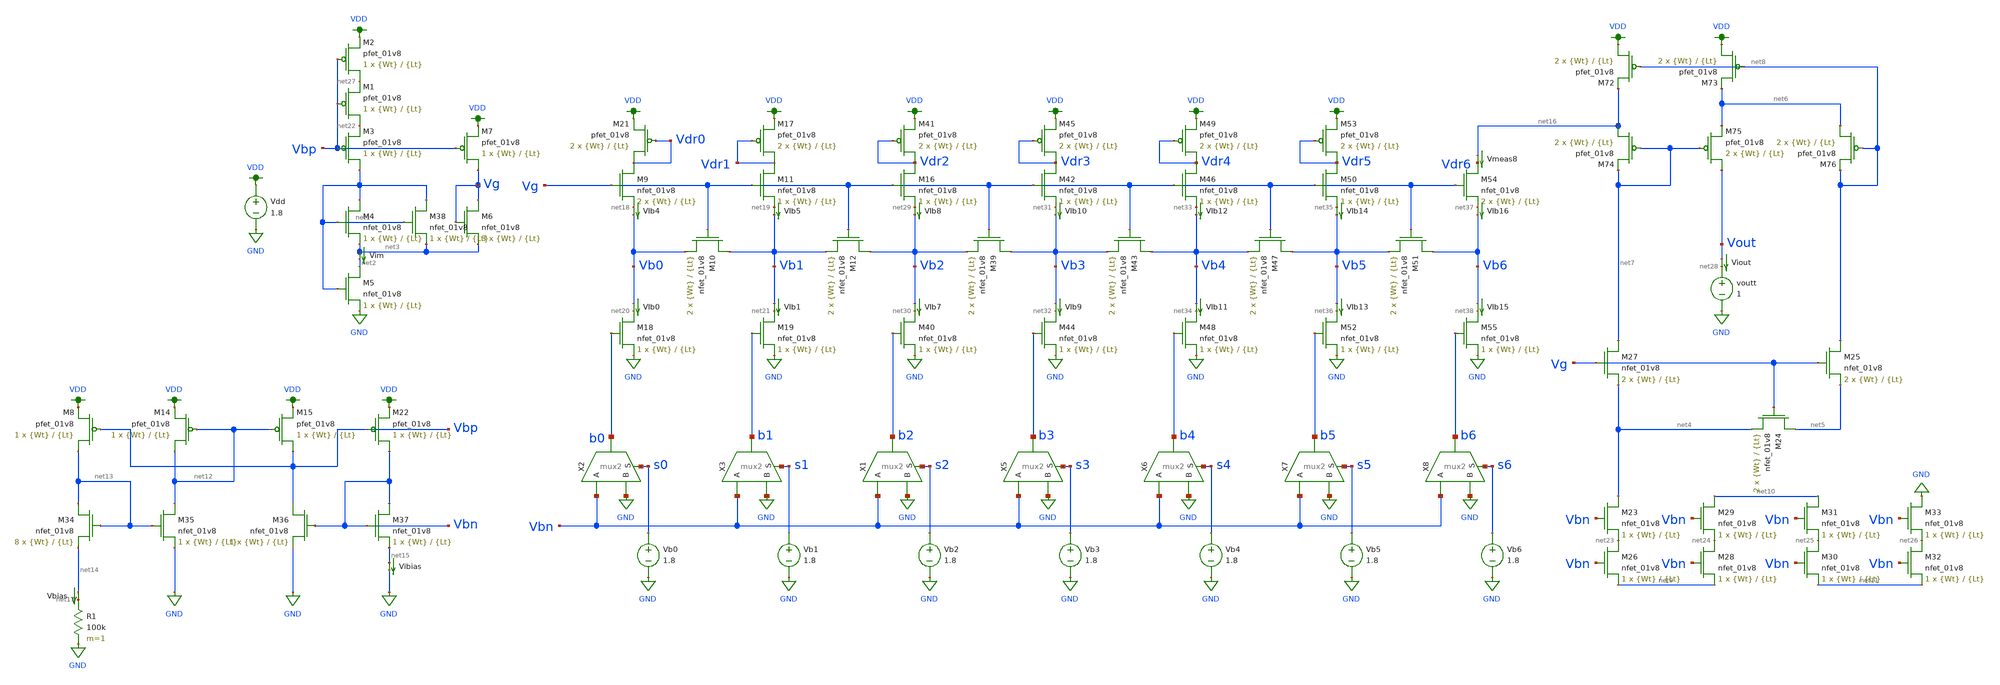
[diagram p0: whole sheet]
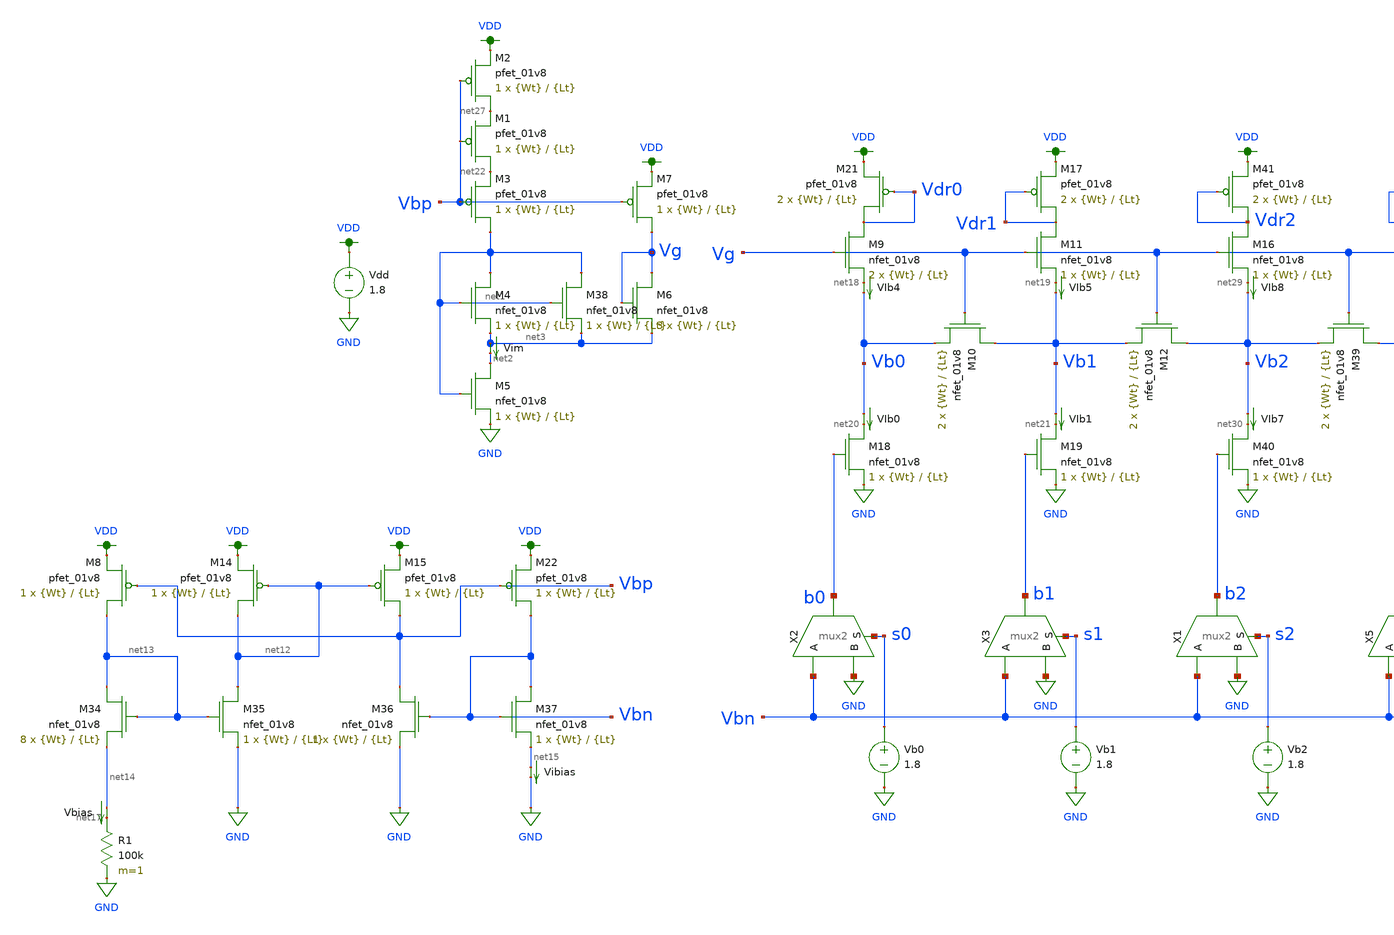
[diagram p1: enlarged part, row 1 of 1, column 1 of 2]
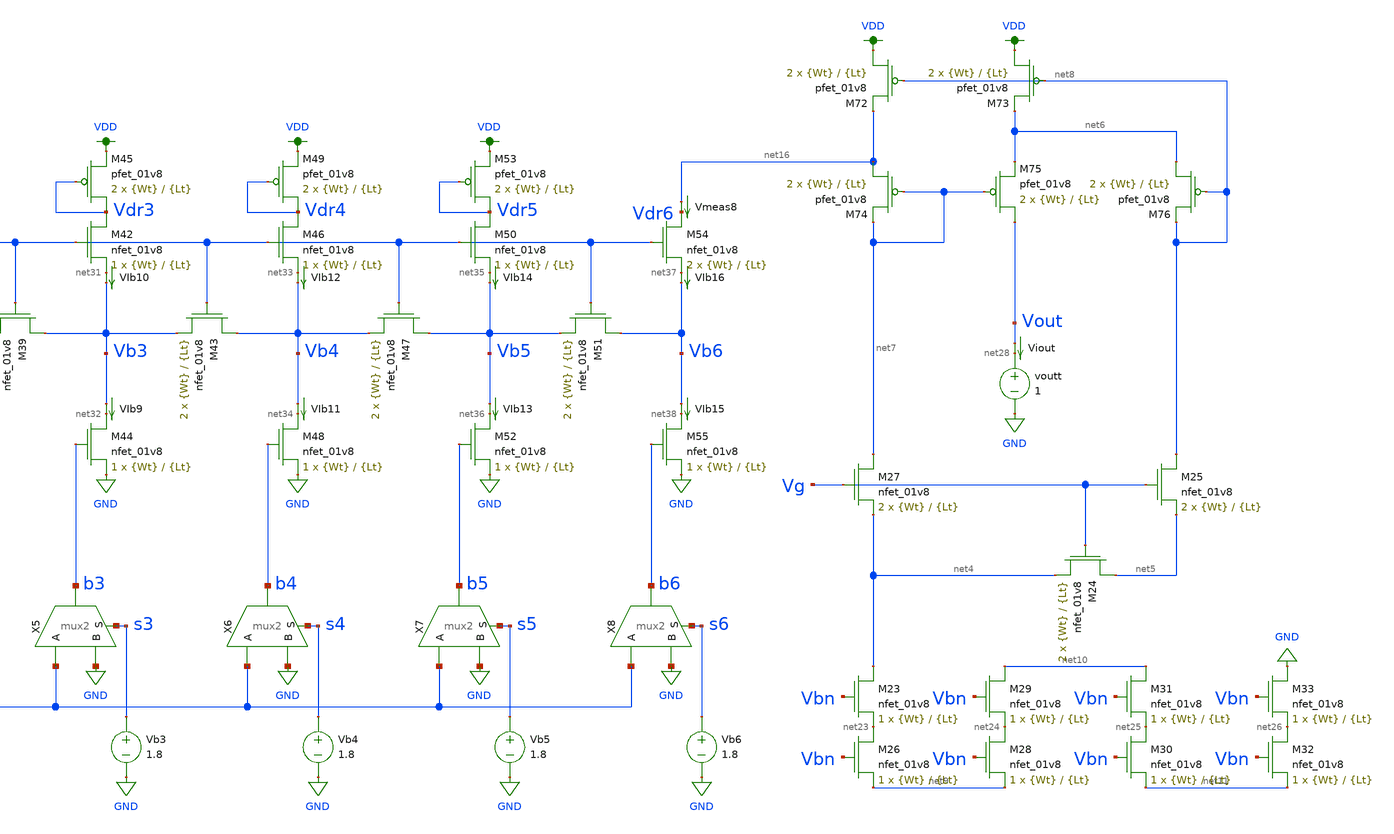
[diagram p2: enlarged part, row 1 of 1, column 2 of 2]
** sch_path: schematic/archive/dac7_test_SL.sch
**.subckt dac7_test_SL
X2 b0 Vbn GND s0 mux2
X3 b1 Vbn GND s1 mux2
R1 net17 GND 100k m=1
Vdd VDD GND 1.8
Vb0 s0 GND 1.8
Vb1 s1 GND 1.8
XM9 Vdr0 Vg net18 GND sky130_fd_pr__nfet_01v8 L={Lt} W={Wt} nf=1 ad='int((nf+1)/2) * W/nf * 0.29' as='int((nf+2)/2) * W/nf * 0.29'
+ pd='2*int((nf+1)/2) * (W/nf + 0.29)' ps='2*int((nf+2)/2) * (W/nf + 0.29)' nrd='0.29 / W' nrs='0.29 / W'
+ sa=0 sb=0 sd=0 mult=2 m=2
XM10 Vb1 Vg Vb0 GND sky130_fd_pr__nfet_01v8 L={Lt} W={Wt} nf=1 ad='int((nf+1)/2) * W/nf * 0.29' as='int((nf+2)/2) * W/nf * 0.29'
+ pd='2*int((nf+1)/2) * (W/nf + 0.29)' ps='2*int((nf+2)/2) * (W/nf + 0.29)' nrd='0.29 / W' nrs='0.29 / W'
+ sa=0 sb=0 sd=0 mult=2 m=2
XM11 Vdr1 Vg net19 GND sky130_fd_pr__nfet_01v8 L={Lt} W={Wt} nf=1 ad='int((nf+1)/2) * W/nf * 0.29' as='int((nf+2)/2) * W/nf * 0.29'
+ pd='2*int((nf+1)/2) * (W/nf + 0.29)' ps='2*int((nf+2)/2) * (W/nf + 0.29)' nrd='0.29 / W' nrs='0.29 / W'
+ sa=0 sb=0 sd=0 mult=1 m=1
XM12 Vb2 Vg Vb1 GND sky130_fd_pr__nfet_01v8 L={Lt} W={Wt} nf=1 ad='int((nf+1)/2) * W/nf * 0.29' as='int((nf+2)/2) * W/nf * 0.29'
+ pd='2*int((nf+1)/2) * (W/nf + 0.29)' ps='2*int((nf+2)/2) * (W/nf + 0.29)' nrd='0.29 / W' nrs='0.29 / W'
+ sa=0 sb=0 sd=0 mult=2 m=2
XM18 net20 b0 GND GND sky130_fd_pr__nfet_01v8 L={Lt} W={Wt} nf=1 ad='int((nf+1)/2) * W/nf * 0.29' as='int((nf+2)/2) * W/nf * 0.29'
+ pd='2*int((nf+1)/2) * (W/nf + 0.29)' ps='2*int((nf+2)/2) * (W/nf + 0.29)' nrd='0.29 / W' nrs='0.29 / W'
+ sa=0 sb=0 sd=0 mult=1 m=1
XM19 net21 b1 GND GND sky130_fd_pr__nfet_01v8 L={Lt} W={Wt} nf=1 ad='int((nf+1)/2) * W/nf * 0.29' as='int((nf+2)/2) * W/nf * 0.29'
+ pd='2*int((nf+1)/2) * (W/nf + 0.29)' ps='2*int((nf+2)/2) * (W/nf + 0.29)' nrd='0.29 / W' nrs='0.29 / W'
+ sa=0 sb=0 sd=0 mult=1 m=1
Vbias net14 net17 0
.save i(vbias)
VIb0 Vb0 net20 0
.save i(vib0)
VIb1 Vb1 net21 0
.save i(vib1)
XM3 net1 Vbp net22 VDD sky130_fd_pr__pfet_01v8 L={Lt} W={Wt} nf=1 ad='int((nf+1)/2) * W/nf * 0.29' as='int((nf+2)/2) * W/nf * 0.29'
+ pd='2*int((nf+1)/2) * (W/nf + 0.29)' ps='2*int((nf+2)/2) * (W/nf + 0.29)' nrd='0.29 / W' nrs='0.29 / W'
+ sa=0 sb=0 sd=0 mult=1 m=1
XM4 net1 net1 net3 GND sky130_fd_pr__nfet_01v8 L={Lt} W={Wt} nf=1 ad='int((nf+1)/2) * W/nf * 0.29' as='int((nf+2)/2) * W/nf * 0.29'
+ pd='2*int((nf+1)/2) * (W/nf + 0.29)' ps='2*int((nf+2)/2) * (W/nf + 0.29)' nrd='0.29 / W' nrs='0.29 / W'
+ sa=0 sb=0 sd=0 mult=1 m=1
XM5 net2 net1 GND GND sky130_fd_pr__nfet_01v8 L={Lt} W={Wt} nf=1 ad='int((nf+1)/2) * W/nf * 0.29' as='int((nf+2)/2) * W/nf * 0.29'
+ pd='2*int((nf+1)/2) * (W/nf + 0.29)' ps='2*int((nf+2)/2) * (W/nf + 0.29)' nrd='0.29 / W' nrs='0.29 / W'
+ sa=0 sb=0 sd=0 mult=1 m=1
Vim net3 net2 0
.save i(vim)
XM6 Vg Vg net3 GND sky130_fd_pr__nfet_01v8 L={Lt} W={Wt} nf=1 ad='int((nf+1)/2) * W/nf * 0.29' as='int((nf+2)/2) * W/nf * 0.29'
+ pd='2*int((nf+1)/2) * (W/nf + 0.29)' ps='2*int((nf+2)/2) * (W/nf + 0.29)' nrd='0.29 / W' nrs='0.29 / W'
+ sa=0 sb=0 sd=0 mult=3 m=3
XM7 Vg Vbp VDD VDD sky130_fd_pr__pfet_01v8 L={Lt} W={Wt} nf=1 ad='int((nf+1)/2) * W/nf * 0.29' as='int((nf+2)/2) * W/nf * 0.29'
+ pd='2*int((nf+1)/2) * (W/nf + 0.29)' ps='2*int((nf+2)/2) * (W/nf + 0.29)' nrd='0.29 / W' nrs='0.29 / W'
+ sa=0 sb=0 sd=0 mult=1 m=1
XM17 Vdr1 Vdr1 VDD VDD sky130_fd_pr__pfet_01v8 L={Lt} W={Wt} nf=1 ad='int((nf+1)/2) * W/nf * 0.29' as='int((nf+2)/2) * W/nf * 0.29'
+ pd='2*int((nf+1)/2) * (W/nf + 0.29)' ps='2*int((nf+2)/2) * (W/nf + 0.29)' nrd='0.29 / W' nrs='0.29 / W'
+ sa=0 sb=0 sd=0 mult=2 m=2
XM21 Vdr0 Vdr0 VDD VDD sky130_fd_pr__pfet_01v8 L={Lt} W={Wt} nf=1 ad='int((nf+1)/2) * W/nf * 0.29' as='int((nf+2)/2) * W/nf * 0.29'
+ pd='2*int((nf+1)/2) * (W/nf + 0.29)' ps='2*int((nf+2)/2) * (W/nf + 0.29)' nrd='0.29 / W' nrs='0.29 / W'
+ sa=0 sb=0 sd=0 mult=2 m=2
VIb4 net18 Vb0 0
.save i(vib4)
VIb5 net19 Vb1 0
.save i(vib5)
XM24 net5 Vg net4 GND sky130_fd_pr__nfet_01v8 L={Lt} W={Wt} nf=1 ad='int((nf+1)/2) * W/nf * 0.29' as='int((nf+2)/2) * W/nf * 0.29'
+ pd='2*int((nf+1)/2) * (W/nf + 0.29)' ps='2*int((nf+2)/2) * (W/nf + 0.29)' nrd='0.29 / W' nrs='0.29 / W'
+ sa=0 sb=0 sd=0 mult=2 m=2
XM25 net8 Vg net5 GND sky130_fd_pr__nfet_01v8 L={Lt} W={Wt} nf=1 ad='int((nf+1)/2) * W/nf * 0.29' as='int((nf+2)/2) * W/nf * 0.29'
+ pd='2*int((nf+1)/2) * (W/nf + 0.29)' ps='2*int((nf+2)/2) * (W/nf + 0.29)' nrd='0.29 / W' nrs='0.29 / W'
+ sa=0 sb=0 sd=0 mult=2 m=2
XM26 net23 Vbn net9 GND sky130_fd_pr__nfet_01v8 L={Lt} W={Wt} nf=1 ad='int((nf+1)/2) * W/nf * 0.29' as='int((nf+2)/2) * W/nf * 0.29'
+ pd='2*int((nf+1)/2) * (W/nf + 0.29)' ps='2*int((nf+2)/2) * (W/nf + 0.29)' nrd='0.29 / W' nrs='0.29 / W'
+ sa=0 sb=0 sd=0 mult=1 m=1
XM27 net7 Vg net4 GND sky130_fd_pr__nfet_01v8 L={Lt} W={Wt} nf=1 ad='int((nf+1)/2) * W/nf * 0.29' as='int((nf+2)/2) * W/nf * 0.29'
+ pd='2*int((nf+1)/2) * (W/nf + 0.29)' ps='2*int((nf+2)/2) * (W/nf + 0.29)' nrd='0.29 / W' nrs='0.29 / W'
+ sa=0 sb=0 sd=0 mult=2 m=2
XM72 VDD net8 net16 VDD sky130_fd_pr__pfet_01v8 L={Lt} W={Wt} nf=1 ad='int((nf+1)/2) * W/nf * 0.29' as='int((nf+2)/2) * W/nf * 0.29'
+ pd='2*int((nf+1)/2) * (W/nf + 0.29)' ps='2*int((nf+2)/2) * (W/nf + 0.29)' nrd='0.29 / W' nrs='0.29 / W'
+ sa=0 sb=0 sd=0 mult=2 m=2
XM73 VDD net8 net6 VDD sky130_fd_pr__pfet_01v8 L={Lt} W={Wt} nf=1 ad='int((nf+1)/2) * W/nf * 0.29' as='int((nf+2)/2) * W/nf * 0.29'
+ pd='2*int((nf+1)/2) * (W/nf + 0.29)' ps='2*int((nf+2)/2) * (W/nf + 0.29)' nrd='0.29 / W' nrs='0.29 / W'
+ sa=0 sb=0 sd=0 mult=2 m=2
XM74 net16 net7 net7 VDD sky130_fd_pr__pfet_01v8 L={Lt} W={Wt} nf=1 ad='int((nf+1)/2) * W/nf * 0.29'
+ as='int((nf+2)/2) * W/nf * 0.29' pd='2*int((nf+1)/2) * (W/nf + 0.29)' ps='2*int((nf+2)/2) * (W/nf + 0.29)'
+ nrd='0.29 / W' nrs='0.29 / W' sa=0 sb=0 sd=0 mult=2 m=2
XM75 Vout net7 net6 VDD sky130_fd_pr__pfet_01v8 L={Lt} W={Wt} nf=1 ad='int((nf+1)/2) * W/nf * 0.29' as='int((nf+2)/2) * W/nf * 0.29'
+ pd='2*int((nf+1)/2) * (W/nf + 0.29)' ps='2*int((nf+2)/2) * (W/nf + 0.29)' nrd='0.29 / W' nrs='0.29 / W'
+ sa=0 sb=0 sd=0 mult=2 m=2
XM76 net6 net8 net8 VDD sky130_fd_pr__pfet_01v8 L={Lt} W={Wt} nf=1 ad='int((nf+1)/2) * W/nf * 0.29' as='int((nf+2)/2) * W/nf * 0.29'
+ pd='2*int((nf+1)/2) * (W/nf + 0.29)' ps='2*int((nf+2)/2) * (W/nf + 0.29)' nrd='0.29 / W' nrs='0.29 / W'
+ sa=0 sb=0 sd=0 mult=2 m=2
XM23 net4 Vbn net23 GND sky130_fd_pr__nfet_01v8 L={Lt} W={Wt} nf=1 ad='int((nf+1)/2) * W/nf * 0.29' as='int((nf+2)/2) * W/nf * 0.29'
+ pd='2*int((nf+1)/2) * (W/nf + 0.29)' ps='2*int((nf+2)/2) * (W/nf + 0.29)' nrd='0.29 / W' nrs='0.29 / W'
+ sa=0 sb=0 sd=0 mult=1 m=1
XM28 net24 Vbn net9 GND sky130_fd_pr__nfet_01v8 L={Lt} W={Wt} nf=1 ad='int((nf+1)/2) * W/nf * 0.29' as='int((nf+2)/2) * W/nf * 0.29'
+ pd='2*int((nf+1)/2) * (W/nf + 0.29)' ps='2*int((nf+2)/2) * (W/nf + 0.29)' nrd='0.29 / W' nrs='0.29 / W'
+ sa=0 sb=0 sd=0 mult=1 m=1
XM29 net10 Vbn net24 GND sky130_fd_pr__nfet_01v8 L={Lt} W={Wt} nf=1 ad='int((nf+1)/2) * W/nf * 0.29'
+ as='int((nf+2)/2) * W/nf * 0.29' pd='2*int((nf+1)/2) * (W/nf + 0.29)' ps='2*int((nf+2)/2) * (W/nf + 0.29)'
+ nrd='0.29 / W' nrs='0.29 / W' sa=0 sb=0 sd=0 mult=1 m=1
XM30 net25 Vbn net11 GND sky130_fd_pr__nfet_01v8 L={Lt} W={Wt} nf=1 ad='int((nf+1)/2) * W/nf * 0.29'
+ as='int((nf+2)/2) * W/nf * 0.29' pd='2*int((nf+1)/2) * (W/nf + 0.29)' ps='2*int((nf+2)/2) * (W/nf + 0.29)'
+ nrd='0.29 / W' nrs='0.29 / W' sa=0 sb=0 sd=0 mult=1 m=1
XM31 net10 Vbn net25 GND sky130_fd_pr__nfet_01v8 L={Lt} W={Wt} nf=1 ad='int((nf+1)/2) * W/nf * 0.29'
+ as='int((nf+2)/2) * W/nf * 0.29' pd='2*int((nf+1)/2) * (W/nf + 0.29)' ps='2*int((nf+2)/2) * (W/nf + 0.29)'
+ nrd='0.29 / W' nrs='0.29 / W' sa=0 sb=0 sd=0 mult=1 m=1
XM32 net26 Vbn net11 GND sky130_fd_pr__nfet_01v8 L={Lt} W={Wt} nf=1 ad='int((nf+1)/2) * W/nf * 0.29'
+ as='int((nf+2)/2) * W/nf * 0.29' pd='2*int((nf+1)/2) * (W/nf + 0.29)' ps='2*int((nf+2)/2) * (W/nf + 0.29)'
+ nrd='0.29 / W' nrs='0.29 / W' sa=0 sb=0 sd=0 mult=1 m=1
XM33 GND Vbn net26 GND sky130_fd_pr__nfet_01v8 L={Lt} W={Wt} nf=1 ad='int((nf+1)/2) * W/nf * 0.29' as='int((nf+2)/2) * W/nf * 0.29'
+ pd='2*int((nf+1)/2) * (W/nf + 0.29)' ps='2*int((nf+2)/2) * (W/nf + 0.29)' nrd='0.29 / W' nrs='0.29 / W'
+ sa=0 sb=0 sd=0 mult=1 m=1
XM8 net13 Vbp VDD VDD sky130_fd_pr__pfet_01v8 L={Lt} W={Wt} nf=1 ad='int((nf+1)/2) * W/nf * 0.29' as='int((nf+2)/2) * W/nf * 0.29'
+ pd='2*int((nf+1)/2) * (W/nf + 0.29)' ps='2*int((nf+2)/2) * (W/nf + 0.29)' nrd='0.29 / W' nrs='0.29 / W'
+ sa=0 sb=0 sd=0 mult=1 m=1
XM14 net12 net12 VDD VDD sky130_fd_pr__pfet_01v8 L={Lt} W={Wt} nf=1 ad='int((nf+1)/2) * W/nf * 0.29'
+ as='int((nf+2)/2) * W/nf * 0.29' pd='2*int((nf+1)/2) * (W/nf + 0.29)' ps='2*int((nf+2)/2) * (W/nf + 0.29)'
+ nrd='0.29 / W' nrs='0.29 / W' sa=0 sb=0 sd=0 mult=1 m=1
XM15 Vbp net12 VDD VDD sky130_fd_pr__pfet_01v8 L={Lt} W={Wt} nf=1 ad='int((nf+1)/2) * W/nf * 0.29' as='int((nf+2)/2) * W/nf * 0.29'
+ pd='2*int((nf+1)/2) * (W/nf + 0.29)' ps='2*int((nf+2)/2) * (W/nf + 0.29)' nrd='0.29 / W' nrs='0.29 / W'
+ sa=0 sb=0 sd=0 mult=1 m=1
XM22 Vbn Vbp VDD VDD sky130_fd_pr__pfet_01v8 L={Lt} W={Wt} nf=1 ad='int((nf+1)/2) * W/nf * 0.29' as='int((nf+2)/2) * W/nf * 0.29'
+ pd='2*int((nf+1)/2) * (W/nf + 0.29)' ps='2*int((nf+2)/2) * (W/nf + 0.29)' nrd='0.29 / W' nrs='0.29 / W'
+ sa=0 sb=0 sd=0 mult=1 m=1
XM34 net13 net13 net14 GND sky130_fd_pr__nfet_01v8 L={Lt} W={Wt} nf=1 ad='int((nf+1)/2) * W/nf * 0.29'
+ as='int((nf+2)/2) * W/nf * 0.29' pd='2*int((nf+1)/2) * (W/nf + 0.29)' ps='2*int((nf+2)/2) * (W/nf + 0.29)'
+ nrd='0.29 / W' nrs='0.29 / W' sa=0 sb=0 sd=0 mult=8 m=8
XM35 net12 net13 GND GND sky130_fd_pr__nfet_01v8 L={Lt} W={Wt} nf=1 ad='int((nf+1)/2) * W/nf * 0.29'
+ as='int((nf+2)/2) * W/nf * 0.29' pd='2*int((nf+1)/2) * (W/nf + 0.29)' ps='2*int((nf+2)/2) * (W/nf + 0.29)'
+ nrd='0.29 / W' nrs='0.29 / W' sa=0 sb=0 sd=0 mult=1 m=1
XM36 Vbp Vbn GND GND sky130_fd_pr__nfet_01v8 L={Lt} W={Wt} nf=1 ad='int((nf+1)/2) * W/nf * 0.29' as='int((nf+2)/2) * W/nf * 0.29'
+ pd='2*int((nf+1)/2) * (W/nf + 0.29)' ps='2*int((nf+2)/2) * (W/nf + 0.29)' nrd='0.29 / W' nrs='0.29 / W'
+ sa=0 sb=0 sd=0 mult=1 m=1
XM37 Vbn Vbn net15 GND sky130_fd_pr__nfet_01v8 L={Lt} W={Wt} nf=1 ad='int((nf+1)/2) * W/nf * 0.29' as='int((nf+2)/2) * W/nf * 0.29'
+ pd='2*int((nf+1)/2) * (W/nf + 0.29)' ps='2*int((nf+2)/2) * (W/nf + 0.29)' nrd='0.29 / W' nrs='0.29 / W'
+ sa=0 sb=0 sd=0 mult=1 m=1
Vibias net15 GND 0
.save i(vibias)
XM1 net22 Vbp net27 VDD sky130_fd_pr__pfet_01v8 L={Lt} W={Wt} nf=1 ad='int((nf+1)/2) * W/nf * 0.29' as='int((nf+2)/2) * W/nf * 0.29'
+ pd='2*int((nf+1)/2) * (W/nf + 0.29)' ps='2*int((nf+2)/2) * (W/nf + 0.29)' nrd='0.29 / W' nrs='0.29 / W'
+ sa=0 sb=0 sd=0 mult=1 m=1
XM2 net27 Vbp VDD VDD sky130_fd_pr__pfet_01v8 L={Lt} W={Wt} nf=1 ad='int((nf+1)/2) * W/nf * 0.29' as='int((nf+2)/2) * W/nf * 0.29'
+ pd='2*int((nf+1)/2) * (W/nf + 0.29)' ps='2*int((nf+2)/2) * (W/nf + 0.29)' nrd='0.29 / W' nrs='0.29 / W'
+ sa=0 sb=0 sd=0 mult=1 m=1
XM38 net1 net1 net3 GND sky130_fd_pr__nfet_01v8 L={Lt} W={Wt} nf=1 ad='int((nf+1)/2) * W/nf * 0.29' as='int((nf+2)/2) * W/nf * 0.29'
+ pd='2*int((nf+1)/2) * (W/nf + 0.29)' ps='2*int((nf+2)/2) * (W/nf + 0.29)' nrd='0.29 / W' nrs='0.29 / W'
+ sa=0 sb=0 sd=0 mult=1 m=1
voutt net28 GND 1
X1 b2 Vbn GND s2 mux2
Vb3 s3 GND 1.8
XM16 Vdr2 Vg net29 GND sky130_fd_pr__nfet_01v8 L={Lt} W={Wt} nf=1 ad='int((nf+1)/2) * W/nf * 0.29' as='int((nf+2)/2) * W/nf * 0.29'
+ pd='2*int((nf+1)/2) * (W/nf + 0.29)' ps='2*int((nf+2)/2) * (W/nf + 0.29)' nrd='0.29 / W' nrs='0.29 / W'
+ sa=0 sb=0 sd=0 mult=1 m=1
XM39 Vb3 Vg Vb2 GND sky130_fd_pr__nfet_01v8 L={Lt} W={Wt} nf=1 ad='int((nf+1)/2) * W/nf * 0.29' as='int((nf+2)/2) * W/nf * 0.29'
+ pd='2*int((nf+1)/2) * (W/nf + 0.29)' ps='2*int((nf+2)/2) * (W/nf + 0.29)' nrd='0.29 / W' nrs='0.29 / W'
+ sa=0 sb=0 sd=0 mult=2 m=2
XM40 net30 b2 GND GND sky130_fd_pr__nfet_01v8 L={Lt} W={Wt} nf=1 ad='int((nf+1)/2) * W/nf * 0.29' as='int((nf+2)/2) * W/nf * 0.29'
+ pd='2*int((nf+1)/2) * (W/nf + 0.29)' ps='2*int((nf+2)/2) * (W/nf + 0.29)' nrd='0.29 / W' nrs='0.29 / W'
+ sa=0 sb=0 sd=0 mult=1 m=1
VIb7 Vb2 net30 0
.save i(vib7)
XM41 Vdr2 Vdr2 VDD VDD sky130_fd_pr__pfet_01v8 L={Lt} W={Wt} nf=1 ad='int((nf+1)/2) * W/nf * 0.29' as='int((nf+2)/2) * W/nf * 0.29'
+ pd='2*int((nf+1)/2) * (W/nf + 0.29)' ps='2*int((nf+2)/2) * (W/nf + 0.29)' nrd='0.29 / W' nrs='0.29 / W'
+ sa=0 sb=0 sd=0 mult=2 m=2
VIb8 net29 Vb2 0
.save i(vib8)
X5 b3 Vbn GND s3 mux2
Vb4 s4 GND 1.8
XM42 Vdr3 Vg net31 GND sky130_fd_pr__nfet_01v8 L={Lt} W={Wt} nf=1 ad='int((nf+1)/2) * W/nf * 0.29' as='int((nf+2)/2) * W/nf * 0.29'
+ pd='2*int((nf+1)/2) * (W/nf + 0.29)' ps='2*int((nf+2)/2) * (W/nf + 0.29)' nrd='0.29 / W' nrs='0.29 / W'
+ sa=0 sb=0 sd=0 mult=1 m=1
XM43 Vb4 Vg Vb3 GND sky130_fd_pr__nfet_01v8 L={Lt} W={Wt} nf=1 ad='int((nf+1)/2) * W/nf * 0.29' as='int((nf+2)/2) * W/nf * 0.29'
+ pd='2*int((nf+1)/2) * (W/nf + 0.29)' ps='2*int((nf+2)/2) * (W/nf + 0.29)' nrd='0.29 / W' nrs='0.29 / W'
+ sa=0 sb=0 sd=0 mult=2 m=2
XM44 net32 b3 GND GND sky130_fd_pr__nfet_01v8 L={Lt} W={Wt} nf=1 ad='int((nf+1)/2) * W/nf * 0.29' as='int((nf+2)/2) * W/nf * 0.29'
+ pd='2*int((nf+1)/2) * (W/nf + 0.29)' ps='2*int((nf+2)/2) * (W/nf + 0.29)' nrd='0.29 / W' nrs='0.29 / W'
+ sa=0 sb=0 sd=0 mult=1 m=1
VIb9 Vb3 net32 0
.save i(vib9)
XM45 Vdr3 Vdr3 VDD VDD sky130_fd_pr__pfet_01v8 L={Lt} W={Wt} nf=1 ad='int((nf+1)/2) * W/nf * 0.29' as='int((nf+2)/2) * W/nf * 0.29'
+ pd='2*int((nf+1)/2) * (W/nf + 0.29)' ps='2*int((nf+2)/2) * (W/nf + 0.29)' nrd='0.29 / W' nrs='0.29 / W'
+ sa=0 sb=0 sd=0 mult=2 m=2
VIb10 net31 Vb3 0
.save i(vib10)
X6 b4 Vbn GND s4 mux2
Vb5 s5 GND 1.8
XM46 Vdr4 Vg net33 GND sky130_fd_pr__nfet_01v8 L={Lt} W={Wt} nf=1 ad='int((nf+1)/2) * W/nf * 0.29' as='int((nf+2)/2) * W/nf * 0.29'
+ pd='2*int((nf+1)/2) * (W/nf + 0.29)' ps='2*int((nf+2)/2) * (W/nf + 0.29)' nrd='0.29 / W' nrs='0.29 / W'
+ sa=0 sb=0 sd=0 mult=1 m=1
XM47 Vb5 Vg Vb4 GND sky130_fd_pr__nfet_01v8 L={Lt} W={Wt} nf=1 ad='int((nf+1)/2) * W/nf * 0.29' as='int((nf+2)/2) * W/nf * 0.29'
+ pd='2*int((nf+1)/2) * (W/nf + 0.29)' ps='2*int((nf+2)/2) * (W/nf + 0.29)' nrd='0.29 / W' nrs='0.29 / W'
+ sa=0 sb=0 sd=0 mult=2 m=2
XM48 net34 b4 GND GND sky130_fd_pr__nfet_01v8 L={Lt} W={Wt} nf=1 ad='int((nf+1)/2) * W/nf * 0.29' as='int((nf+2)/2) * W/nf * 0.29'
+ pd='2*int((nf+1)/2) * (W/nf + 0.29)' ps='2*int((nf+2)/2) * (W/nf + 0.29)' nrd='0.29 / W' nrs='0.29 / W'
+ sa=0 sb=0 sd=0 mult=1 m=1
VIb11 Vb4 net34 0
.save i(vib11)
XM49 Vdr4 Vdr4 VDD VDD sky130_fd_pr__pfet_01v8 L={Lt} W={Wt} nf=1 ad='int((nf+1)/2) * W/nf * 0.29' as='int((nf+2)/2) * W/nf * 0.29'
+ pd='2*int((nf+1)/2) * (W/nf + 0.29)' ps='2*int((nf+2)/2) * (W/nf + 0.29)' nrd='0.29 / W' nrs='0.29 / W'
+ sa=0 sb=0 sd=0 mult=2 m=2
VIb12 net33 Vb4 0
.save i(vib12)
X7 b5 Vbn GND s5 mux2
Vb6 s6 GND 1.8
XM50 Vdr5 Vg net35 GND sky130_fd_pr__nfet_01v8 L={Lt} W={Wt} nf=1 ad='int((nf+1)/2) * W/nf * 0.29' as='int((nf+2)/2) * W/nf * 0.29'
+ pd='2*int((nf+1)/2) * (W/nf + 0.29)' ps='2*int((nf+2)/2) * (W/nf + 0.29)' nrd='0.29 / W' nrs='0.29 / W'
+ sa=0 sb=0 sd=0 mult=1 m=1
XM51 Vb6 Vg Vb5 GND sky130_fd_pr__nfet_01v8 L={Lt} W={Wt} nf=1 ad='int((nf+1)/2) * W/nf * 0.29' as='int((nf+2)/2) * W/nf * 0.29'
+ pd='2*int((nf+1)/2) * (W/nf + 0.29)' ps='2*int((nf+2)/2) * (W/nf + 0.29)' nrd='0.29 / W' nrs='0.29 / W'
+ sa=0 sb=0 sd=0 mult=2 m=2
XM52 net36 b5 GND GND sky130_fd_pr__nfet_01v8 L={Lt} W={Wt} nf=1 ad='int((nf+1)/2) * W/nf * 0.29' as='int((nf+2)/2) * W/nf * 0.29'
+ pd='2*int((nf+1)/2) * (W/nf + 0.29)' ps='2*int((nf+2)/2) * (W/nf + 0.29)' nrd='0.29 / W' nrs='0.29 / W'
+ sa=0 sb=0 sd=0 mult=1 m=1
VIb13 Vb5 net36 0
.save i(vib13)
XM53 Vdr5 Vdr5 VDD VDD sky130_fd_pr__pfet_01v8 L={Lt} W={Wt} nf=1 ad='int((nf+1)/2) * W/nf * 0.29' as='int((nf+2)/2) * W/nf * 0.29'
+ pd='2*int((nf+1)/2) * (W/nf + 0.29)' ps='2*int((nf+2)/2) * (W/nf + 0.29)' nrd='0.29 / W' nrs='0.29 / W'
+ sa=0 sb=0 sd=0 mult=2 m=2
VIb14 net35 Vb5 0
.save i(vib14)
X8 b6 Vbn GND s6 mux2
XM54 Vdr6 Vg net37 GND sky130_fd_pr__nfet_01v8 L={Lt} W={Wt} nf=1 ad='int((nf+1)/2) * W/nf * 0.29' as='int((nf+2)/2) * W/nf * 0.29'
+ pd='2*int((nf+1)/2) * (W/nf + 0.29)' ps='2*int((nf+2)/2) * (W/nf + 0.29)' nrd='0.29 / W' nrs='0.29 / W'
+ sa=0 sb=0 sd=0 mult=2 m=2
XM55 net38 b6 GND GND sky130_fd_pr__nfet_01v8 L={Lt} W={Wt} nf=1 ad='int((nf+1)/2) * W/nf * 0.29' as='int((nf+2)/2) * W/nf * 0.29'
+ pd='2*int((nf+1)/2) * (W/nf + 0.29)' ps='2*int((nf+2)/2) * (W/nf + 0.29)' nrd='0.29 / W' nrs='0.29 / W'
+ sa=0 sb=0 sd=0 mult=1 m=1
Vmeas8 net16 Vdr6 0
.save i(vmeas8)
VIb15 Vb6 net38 0
.save i(vib15)
VIb16 net37 Vb6 0
.save i(vib16)
Vb2 s2 GND 1.8
Viout Vout net28 0
.save i(viout)
**** begin user architecture code

.option wnflag=1
.param MC_SWITCH=1.0
.lib ~/skywater/skywater-pdk/libraries/sky130_fd_pr_ngspice/latest/models/sky130.lib.spice tt


.param Wt = 3
.param Lt = 1
.control
*** change W and L for the next two lines as well !***
  let myW = 3
  let myL = 1
  set wr_singlescale
  let runs = 10
  let run = 1
  while run <= runs
    set appendwrite = FALSE
    set wr_vecnames
    let code = 0
    while code < 32
      if code eq 0
        let b0 = 0
      else
        let b0 = (code % 2) * 1.8
      end
      if floor(code / 2) eq 0
        let b1 = 0
      else
        let b1 = (floor(code / 2) % 2) * 1.8
      end
      if floor(code / 4) eq 0
        let b2 = 0
      else
        let b2 = (floor(code / 4) % 2) * 1.8
      end
      if floor(code / 8) eq 0
        let b3 = 0
      else
        let b3 = floor(code / 8) % 2 * 1.8
      end
      if floor(code / 16) eq 0
        let b4 = 0
      else
        let b4 = floor(code / 16) % 2 * 1.8
      end
      if floor(code / 32) eq 0
        let b5 = 0
      else
        let b5 = floor(code / 32) % 2 * 1.8
      end
      if floor(code / 64) eq 0
        let b6 = 0
      else
        let b6 = floor(code / 64) % 2 * 1.8
      end
      alter vb0 $&b0
      alter vb1 $&b1
      alter vb2 $&b2
      alter vb3 $&b3
      alter vb4 $&b4
      alter vb5 $&b5
      alter vb6 $&b6
      save v(b0) v(b1) v(b2) v(b3) v(b4) v(b5) v(b6) i(vbias) i(viout) v(vout)
      op
      wrdata ~/Documents/MADVLSI-MP4/schematic/data/dac7_L{$&myL}W{$&myW}op-{$&run}.txt v(b0) v(b1) v(b2)
+ v(b3) v(b4) v(b5) v(b6) i(vbias) i(viout) v(vout)
      if code eq 0
        set appendwrite
        set wr_vecnames = FALSE
      end
      let code = code + 1
    end
    reset
    let run = run + 1
  end

  set appendwrite = FALSE
  reset
  set wr_singlescale
  set wr_vecnames
  alter vb0 1.8
  alter vb1 1.8
  alter vb2 1.8
  alter vb3 1.8
  alter vb4 1.8
  alter vb5 1.8
  alter vb6 1.8
  save v(b0) v(b1) v(b2) v(b3) v(b4) v(b5) v(b6) i(vbias) i(viout) v(vout)
  dc Voutt 0 1.8 0.01
  run
  wrdata ~/Documents/MADVLSI-MP4/schematic/data/dac7_L{$&myL}W{$&myW}vout-1.txt v(b0) v(b1) v(b2) v(b3)
+ v(b4) v(b5) v(b6) i(vbias) i(viout) v(vout)

  reset
  set wr_singlescale
  set wr_vecnames
  alter vb0 1.8
  alter vb1 1.8
  alter vb2 1.8
  alter vb3 1.8
  alter vb4 1.8
  alter vb5 1.8
  alter vb6 0
  save v(b0) v(b1) v(b2) v(b3) v(b4) v(b5) v(b6) i(vbias) i(viout) v(vout)
  dc Voutt 0 1.8 0.01
  run
  wrdata ~/Documents/MADVLSI-MP4/schematic/data/dac7_L{$&myL}W{$&myW}vout-2.txt v(b0) v(b1) v(b2) v(b3)
+ v(b4) v(b5) v(b6) i(vbias) i(viout) v(vout)

  reset
  set wr_singlescale
  set wr_vecnames
  alter vb0 1.8
  alter vb1 1.8
  alter vb2 1.8
  alter vb3 1.8
  alter vb4 1.8
  alter vb5 1.8
  alter vb6 1.8
  save v(b0) v(b1) v(b2) v(b3) v(b4) v(b5) v(b6) i(vbias) i(viout) v(vout)
  dc Voutt 0 1.8 0.01
  run
  wrdata ~/Documents/MADVLSI-MP4/schematic/data/dac7_L{$&myL}W{$&myW}vdd-1.txt v(b0) v(b1) v(b2) v(b3)
+ v(b4) v(b5) v(b6) i(vbias) i(viout) v(vout)

  reset
  set wr_singlescale
  set wr_vecnames
  alter vb0 1.8
  alter vb1 1.8
  alter vb2 1.8
  alter vb3 1.8
  alter vb4 1.8
  alter vb5 1.8
  alter vb6 0
  save v(b0) v(b1) v(b2) v(b3) v(b4) v(b5) v(b6) i(vbias) i(viout) v(vout)
  dc Voutt 0 1.8 0.01
  run
  wrdata ~/Documents/MADVLSI-MP4/schematic/data/dac7_L{$&myL}W{$&myW}vdd-2.txt v(b0) v(b1) v(b2) v(b3)
+ v(b4) v(b5) v(b6) i(vbias) i(viout) v(vout)
.endc

**** end user architecture code
**.ends
.GLOBAL GND
.GLOBAL VDD
.end
